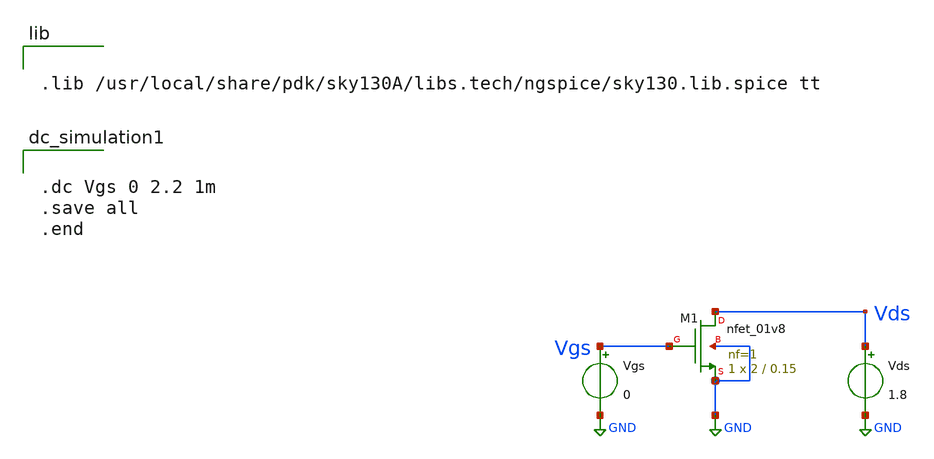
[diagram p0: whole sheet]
** sch_path: xschem/nmosTrait.sch
**.subckt nmosTrait
XM1 Vds Vgs GND GND sky130_fd_pr__nfet_01v8 L=0.15 W=2 nf=1 ad='int((nf+1)/2) * W/nf * 0.29' as='int((nf+2)/2) * W/nf * 0.29'
+ pd='2*int((nf+1)/2) * (W/nf + 0.29)' ps='2*int((nf+2)/2) * (W/nf + 0.29)' nrd='0.29 / W' nrs='0.29 / W'
+ sa=0 sb=0 sd=0 mult=1 m=1
Vgs Vgs GND 0
Vds Vds GND 1.8
**** begin user architecture code


.lib /usr/local/share/pdk/sky130A/libs.tech/ngspice/sky130.lib.spice tt




.dc Vgs 0 2.2 1m
.save all
.end


**** end user architecture code
**.ends
.GLOBAL GND
.end
